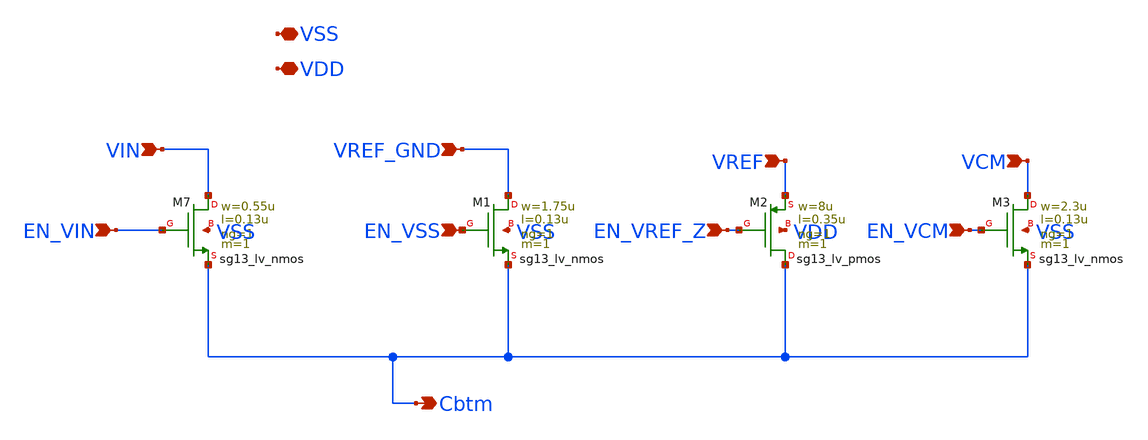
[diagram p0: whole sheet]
** sch_path: schematic/individual_switches/switch_C6.sch
**.subckt switch_C6 VIN EN_VIN VREF_GND EN_VSS Cbtm VSS VREF EN_VREF_Z EN_VCM VCM VDD
*.ipin VIN
*.ipin EN_VIN
*.ipin VREF_GND
*.ipin EN_VSS
*.opin Cbtm
*.iopin VSS
*.ipin VREF
*.ipin EN_VREF_Z
*.ipin EN_VCM
*.ipin VCM
*.iopin VDD
XM7 VIN EN_VIN Cbtm VSS sg13_lv_nmos w=0.55u l=0.13u ng=1 m=1 mm_ok=1
XM1 VREF_GND EN_VSS Cbtm VSS sg13_lv_nmos w=1.75u l=0.13u ng=1 m=1 mm_ok=1
XM2 Cbtm EN_VREF_Z VREF VDD sg13_lv_pmos w=8u l=0.35u ng=1 m=1 mm_ok=1
XM3 VCM EN_VCM Cbtm VSS sg13_lv_nmos w=2.3u l=0.13u ng=1 m=1 mm_ok=1
**.ends
.end
